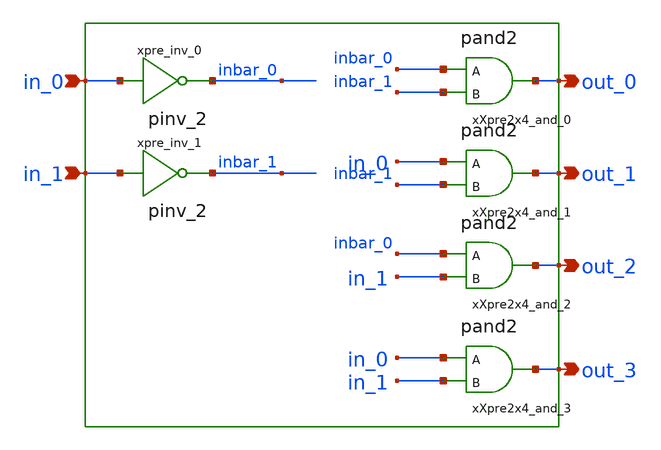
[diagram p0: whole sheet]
** sch_path: sram_2_64_scn4m/hierarchical_predecode2x4_0.sch
**.subckt hierarchical_predecode2x4_0 in_0 in_1 out_0 out_1 out_2 out_3
*.ipin in_0
*.ipin in_1
*.opin out_0
*.opin out_1
*.opin out_2
*.opin out_3
xpre_inv_0 in_0 inbar_0 vdd gnd pinv_2
xpre_inv_1 in_1 inbar_1 vdd gnd pinv_2
xXpre2x4_and_0 inbar_0 inbar_1 out_0 vdd gnd pand2
xXpre2x4_and_1 in_0 inbar_1 out_1 vdd gnd pand2
xXpre2x4_and_2 inbar_0 in_1 out_2 vdd gnd pand2
xXpre2x4_and_3 in_0 in_1 out_3 vdd gnd pand2
**.ends

* expanding   symbol:  pinv_2.sym # of pins=2
** sym_path: sram_2_64_scn4m/pinv_2.sym
** sch_path: sram_2_64_scn4m/pinv_2.sch
.subckt pinv_2 A Z vdd gnd
*.ipin A
*.opin Z
XMpinv_nmos Z A gnd gnd sky130_fd_pr__nfet_01v8 L=0.4 W=0.8 nf=1 ad='int((nf+1)/2) * W/nf * 0.29' as='int((nf+2)/2) * W/nf * 0.29'
+ pd='2*int((nf+1)/2) * (W/nf + 0.29)' ps='2*int((nf+2)/2) * (W/nf + 0.29)' nrd='0.29 / W' nrs='0.29 / W'
+ sa=0 sb=0 sd=0 mult=1 m=1
XMp_inv_pmos Z A vdd vdd sky130_fd_pr__pfet_01v8 L=0.4 W=1.6 nf=1 ad='int((nf+1)/2) * W/nf * 0.29' as='int((nf+2)/2) * W/nf * 0.29'
+ pd='2*int((nf+1)/2) * (W/nf + 0.29)' ps='2*int((nf+2)/2) * (W/nf + 0.29)' nrd='0.29 / W' nrs='0.29 / W'
+ sa=0 sb=0 sd=0 mult=1 m=1
.ends


* expanding   symbol:  pand2.sym # of pins=3
** sym_path: sram_2_16_scn4m/pand2.sym
** sch_path: sram_2_16_scn4m/pand2.sch
.subckt pand2 A B Z vdd gnd
*.ipin A
*.ipin B
*.opin Z
xpand2_nand A B zb_int vdd gnd pnand2_0
xpand2_inv zb_int Z vdd gnd pdriver
**** begin user architecture code


**** end user architecture code
.ends


* expanding   symbol:  pnand2_0.sym # of pins=3
** sym_path: sram_2_16_scn4m/pnand2_0.sym
** sch_path: sram_2_16_scn4m/pnand2_0.sch
.subckt pnand2_0 A B Z vdd gnd
*.ipin A
*.ipin B
*.opin Z
*.iopin vdd
*.iopin gnd
XMpnand2_nmos1 Z B net1 gnd sky130_fd_pr__nfet_01v8 L=0.4 W=1.6 nf=1 ad='int((nf+1)/2) * W/nf * 0.29'
+ as='int((nf+2)/2) * W/nf * 0.29' pd='2*int((nf+1)/2) * (W/nf + 0.29)' ps='2*int((nf+2)/2) * (W/nf + 0.29)'
+ nrd='0.29 / W' nrs='0.29 / W' sa=0 sb=0 sd=0 mult=1 m=1
XMpnand2_pmos1 Z A vdd vdd sky130_fd_pr__pfet_01v8 L=0.4 W=1.6 nf=1 ad='int((nf+1)/2) * W/nf * 0.29'
+ as='int((nf+2)/2) * W/nf * 0.29' pd='2*int((nf+1)/2) * (W/nf + 0.29)' ps='2*int((nf+2)/2) * (W/nf + 0.29)'
+ nrd='0.29 / W' nrs='0.29 / W' sa=0 sb=0 sd=0 mult=1 m=1
XMpnand2_pmos2 Z B vdd vdd sky130_fd_pr__pfet_01v8 L=0.4 W=1.6 nf=1 ad='int((nf+1)/2) * W/nf * 0.29'
+ as='int((nf+2)/2) * W/nf * 0.29' pd='2*int((nf+1)/2) * (W/nf + 0.29)' ps='2*int((nf+2)/2) * (W/nf + 0.29)'
+ nrd='0.29 / W' nrs='0.29 / W' sa=0 sb=0 sd=0 mult=1 m=1
XMpnand2_nmos2 net1 A gnd gnd sky130_fd_pr__nfet_01v8 L=0.4 W=1.6 nf=1 ad='int((nf+1)/2) * W/nf * 0.29'
+ as='int((nf+2)/2) * W/nf * 0.29' pd='2*int((nf+1)/2) * (W/nf + 0.29)' ps='2*int((nf+2)/2) * (W/nf + 0.29)'
+ nrd='0.29 / W' nrs='0.29 / W' sa=0 sb=0 sd=0 mult=1 m=1
.ends


* expanding   symbol:  pdriver.sym # of pins=2
** sym_path: sram_4_16_scn4m/pdriver.sym
** sch_path: sram_4_16_scn4m/pdriver.sch
.subckt pdriver A Z vdd gnd
*.ipin A
*.opin Z
xbuf_inv1 A Z vdd gnd pinv_2
.ends

.end
